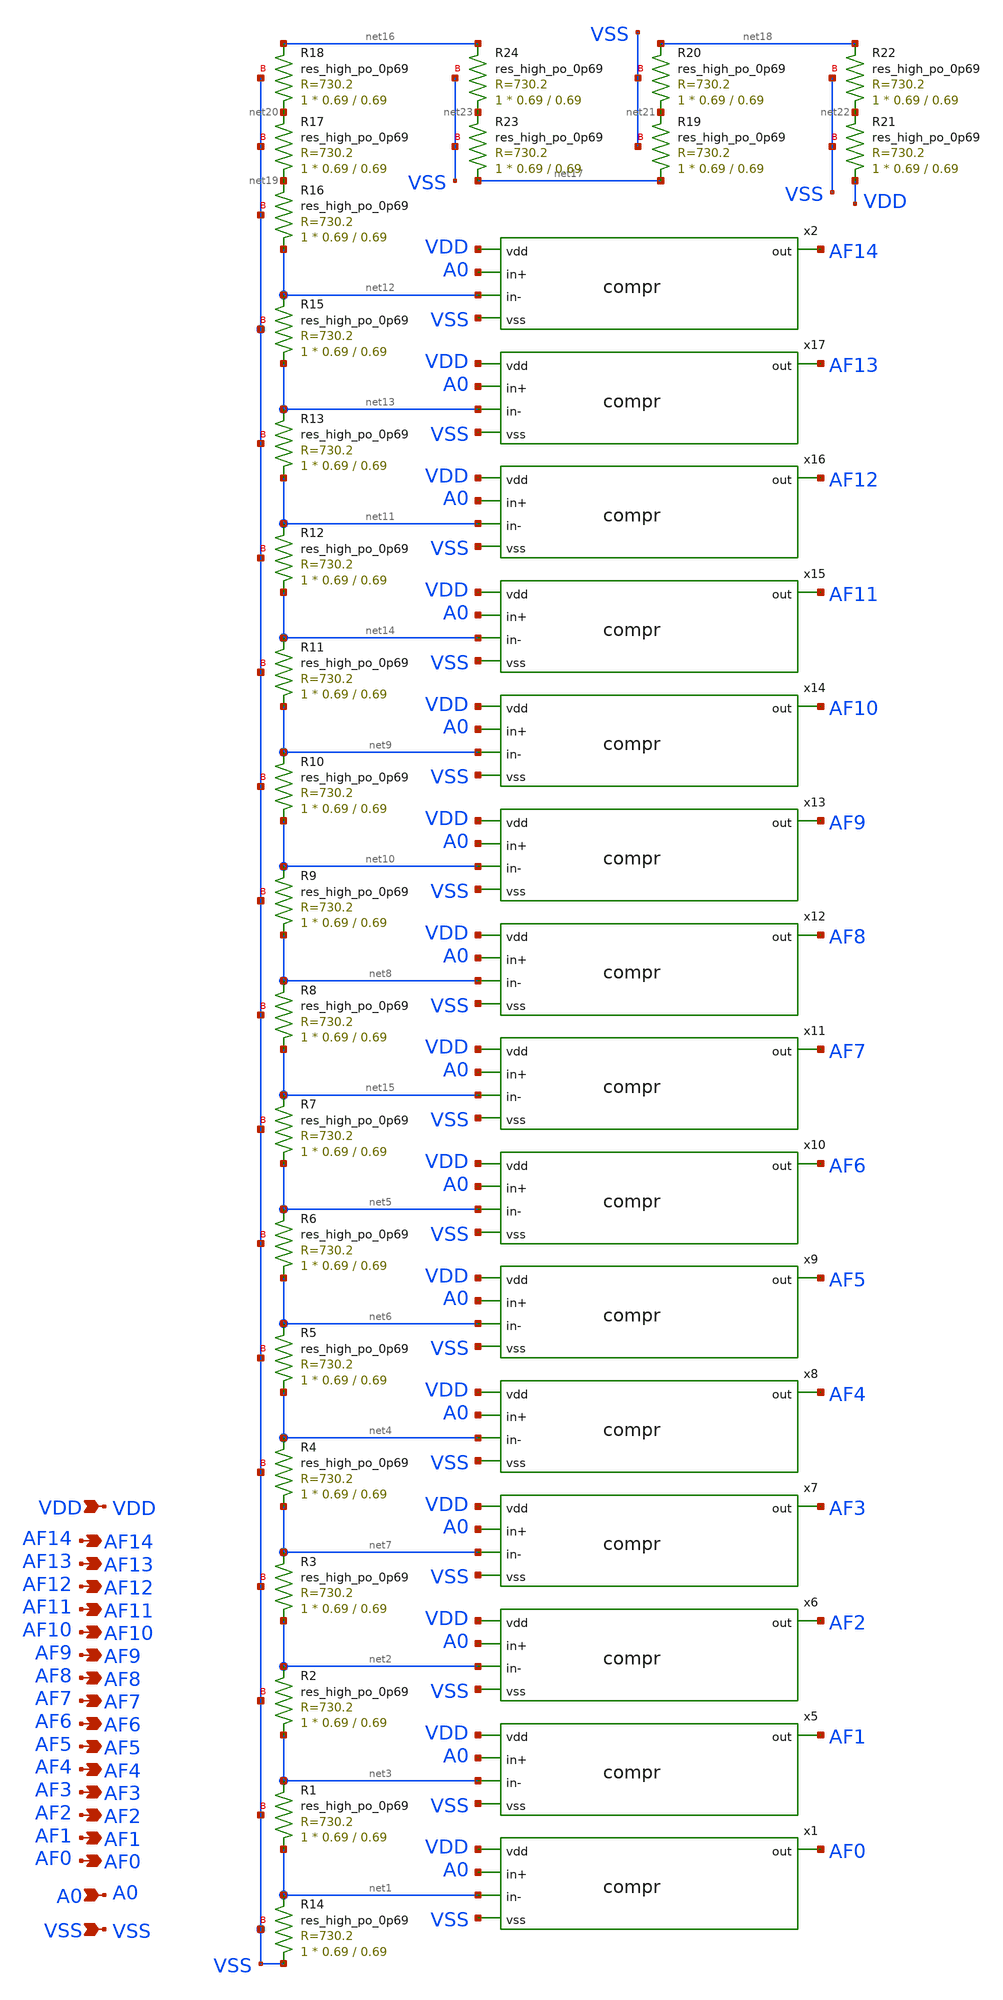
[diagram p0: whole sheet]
** sch_path: xschem/flash_adc.sch
**.subckt flash_adc VDD VSS A0 AF3 AF2 AF1 AF0 AF7 AF6 AF5 AF4 AF11 AF10 AF9 AF8 AF14 AF13 AF12
*.ipin VDD
*.ipin VSS
*.ipin A0
*.opin AF3
*.opin AF2
*.opin AF1
*.opin AF0
*.opin AF7
*.opin AF6
*.opin AF5
*.opin AF4
*.opin AF11
*.opin AF10
*.opin AF9
*.opin AF8
*.opin AF14
*.opin AF13
*.opin AF12
XR14 VSS net1 VSS sky130_fd_pr__res_high_po_0p69 L=0.69 mult=1 m=1
x5 AF1 VDD A0 net3 VSS compr
XR1 net1 net3 VSS sky130_fd_pr__res_high_po_0p69 L=0.69 mult=1 m=1
x6 AF2 VDD A0 net2 VSS compr
XR2 net3 net2 VSS sky130_fd_pr__res_high_po_0p69 L=0.69 mult=1 m=1
x7 AF3 VDD A0 net7 VSS compr
XR3 net2 net7 VSS sky130_fd_pr__res_high_po_0p69 L=0.69 mult=1 m=1
x8 AF4 VDD A0 net4 VSS compr
XR4 net7 net4 VSS sky130_fd_pr__res_high_po_0p69 L=0.69 mult=1 m=1
x9 AF5 VDD A0 net6 VSS compr
XR5 net4 net6 VSS sky130_fd_pr__res_high_po_0p69 L=0.69 mult=1 m=1
x10 AF6 VDD A0 net5 VSS compr
XR6 net6 net5 VSS sky130_fd_pr__res_high_po_0p69 L=0.69 mult=1 m=1
x11 AF7 VDD A0 net15 VSS compr
XR7 net5 net15 VSS sky130_fd_pr__res_high_po_0p69 L=0.69 mult=1 m=1
x12 AF8 VDD A0 net8 VSS compr
XR8 net15 net8 VSS sky130_fd_pr__res_high_po_0p69 L=0.69 mult=1 m=1
x13 AF9 VDD A0 net10 VSS compr
XR9 net8 net10 VSS sky130_fd_pr__res_high_po_0p69 L=0.69 mult=1 m=1
x14 AF10 VDD A0 net9 VSS compr
XR10 net10 net9 VSS sky130_fd_pr__res_high_po_0p69 L=0.69 mult=1 m=1
x15 AF11 VDD A0 net14 VSS compr
XR11 net9 net14 VSS sky130_fd_pr__res_high_po_0p69 L=0.69 mult=1 m=1
x16 AF12 VDD A0 net11 VSS compr
XR12 net14 net11 VSS sky130_fd_pr__res_high_po_0p69 L=0.69 mult=1 m=1
x17 AF13 VDD A0 net13 VSS compr
XR13 net11 net13 VSS sky130_fd_pr__res_high_po_0p69 L=0.69 mult=1 m=1
XR15 net13 net12 VSS sky130_fd_pr__res_high_po_0p69 L=0.69 mult=1 m=1
XR16 net12 net19 VSS sky130_fd_pr__res_high_po_0p69 L=0.69 mult=1 m=1
XR17 net19 net20 VSS sky130_fd_pr__res_high_po_0p69 L=0.69 mult=1 m=1
XR18 net20 net16 VSS sky130_fd_pr__res_high_po_0p69 L=0.69 mult=1 m=1
XR19 net17 net21 VSS sky130_fd_pr__res_high_po_0p69 L=0.69 mult=1 m=1
XR20 net21 net18 VSS sky130_fd_pr__res_high_po_0p69 L=0.69 mult=1 m=1
XR21 VDD net22 VSS sky130_fd_pr__res_high_po_0p69 L=0.69 mult=1 m=1
XR22 net22 net18 VSS sky130_fd_pr__res_high_po_0p69 L=0.69 mult=1 m=1
XR23 net17 net23 VSS sky130_fd_pr__res_high_po_0p69 L=0.69 mult=1 m=1
XR24 net23 net16 VSS sky130_fd_pr__res_high_po_0p69 L=0.69 mult=1 m=1
x1 AF0 VDD A0 net1 VSS compr
x2 AF14 VDD A0 net12 VSS compr
**.ends

* expanding   symbol:  /home/ttuser/Documents/adc_dac_ter_alu/src/xschem/compr.sym # of pins=5
** sym_path: /home/ttuser/Documents/adc_dac_ter_alu/src/xschem/compr.sym
** sch_path: /home/ttuser/Documents/adc_dac_ter_alu/src/xschem/compr.sch
.subckt compr out vdd in+ in- vss
*.ipin IN+
*.opin OUT
*.ipin IN-
*.ipin VDD
*.ipin VSS
XM1 VSS net2 net2 VSS sky130_fd_pr__nfet_01v8_lvt L=4 W=2 nf=1 ad='int((nf+1)/2) * W/nf * 0.29' as='int((nf+2)/2) * W/nf * 0.29'
+ pd='2*int((nf+1)/2) * (W/nf + 0.29)' ps='2*int((nf+2)/2) * (W/nf + 0.29)' nrd='0.29 / W' nrs='0.29 / W'
+ sa=0 sb=0 sd=0 mult=1 m=1
XM2 VSS g1 g1 VSS sky130_fd_pr__nfet_01v8_lvt L=4 W=2 nf=1 ad='int((nf+1)/2) * W/nf * 0.29' as='int((nf+2)/2) * W/nf * 0.29'
+ pd='2*int((nf+1)/2) * (W/nf + 0.29)' ps='2*int((nf+2)/2) * (W/nf + 0.29)' nrd='0.29 / W' nrs='0.29 / W'
+ sa=0 sb=0 sd=0 mult=1 m=1
XM3 VSS net2 net4 VSS sky130_fd_pr__nfet_01v8_lvt L=4 W=2 nf=1 ad='int((nf+1)/2) * W/nf * 0.29' as='int((nf+2)/2) * W/nf * 0.29'
+ pd='2*int((nf+1)/2) * (W/nf + 0.29)' ps='2*int((nf+2)/2) * (W/nf + 0.29)' nrd='0.29 / W' nrs='0.29 / W'
+ sa=0 sb=0 sd=0 mult=1 m=1
XM4 VSS g1 net3 VSS sky130_fd_pr__nfet_01v8_lvt L=4 W=2 nf=1 ad='int((nf+1)/2) * W/nf * 0.29' as='int((nf+2)/2) * W/nf * 0.29'
+ pd='2*int((nf+1)/2) * (W/nf + 0.29)' ps='2*int((nf+2)/2) * (W/nf + 0.29)' nrd='0.29 / W' nrs='0.29 / W'
+ sa=0 sb=0 sd=0 mult=1 m=1
XM5 net2 IN+ net1 VDD sky130_fd_pr__pfet_01v8_lvt L=2 W=8 nf=1 ad='int((nf+1)/2) * W/nf * 0.29' as='int((nf+2)/2) * W/nf * 0.29'
+ pd='2*int((nf+1)/2) * (W/nf + 0.29)' ps='2*int((nf+2)/2) * (W/nf + 0.29)' nrd='0.29 / W' nrs='0.29 / W'
+ sa=0 sb=0 sd=0 mult=1 m=1
XM6 g1 IN- net1 VDD sky130_fd_pr__pfet_01v8_lvt L=2 W=8 nf=1 ad='int((nf+1)/2) * W/nf * 0.29' as='int((nf+2)/2) * W/nf * 0.29'
+ pd='2*int((nf+1)/2) * (W/nf + 0.29)' ps='2*int((nf+2)/2) * (W/nf + 0.29)' nrd='0.29 / W' nrs='0.29 / W'
+ sa=0 sb=0 sd=0 mult=1 m=1
XM7 net4 net3 net5 VDD sky130_fd_pr__pfet_01v8_lvt L=4 W=4 nf=1 ad='int((nf+1)/2) * W/nf * 0.29' as='int((nf+2)/2) * W/nf * 0.29'
+ pd='2*int((nf+1)/2) * (W/nf + 0.29)' ps='2*int((nf+2)/2) * (W/nf + 0.29)' nrd='0.29 / W' nrs='0.29 / W'
+ sa=0 sb=0 sd=0 mult=1 m=1
XM9 net3 net3 net5 VDD sky130_fd_pr__pfet_01v8_lvt L=4 W=4 nf=1 ad='int((nf+1)/2) * W/nf * 0.29' as='int((nf+2)/2) * W/nf * 0.29'
+ pd='2*int((nf+1)/2) * (W/nf + 0.29)' ps='2*int((nf+2)/2) * (W/nf + 0.29)' nrd='0.29 / W' nrs='0.29 / W'
+ sa=0 sb=0 sd=0 mult=1 m=1
XM8 net1 VSS VDD VDD sky130_fd_pr__pfet_01v8 L=8 W=2 nf=1 ad='int((nf+1)/2) * W/nf * 0.29' as='int((nf+2)/2) * W/nf * 0.29'
+ pd='2*int((nf+1)/2) * (W/nf + 0.29)' ps='2*int((nf+2)/2) * (W/nf + 0.29)' nrd='0.29 / W' nrs='0.29 / W'
+ sa=0 sb=0 sd=0 mult=1 m=1
XM10 net5 VSS VDD VDD sky130_fd_pr__pfet_01v8 L=0.15 W=5 nf=1 ad='int((nf+1)/2) * W/nf * 0.29' as='int((nf+2)/2) * W/nf * 0.29'
+ pd='2*int((nf+1)/2) * (W/nf + 0.29)' ps='2*int((nf+2)/2) * (W/nf + 0.29)' nrd='0.29 / W' nrs='0.29 / W'
+ sa=0 sb=0 sd=0 mult=1 m=1
XM14 OUT net6 VSS VSS sky130_fd_pr__nfet_01v8 L=0.15 W=2 nf=1 ad='int((nf+1)/2) * W/nf * 0.29' as='int((nf+2)/2) * W/nf * 0.29'
+ pd='2*int((nf+1)/2) * (W/nf + 0.29)' ps='2*int((nf+2)/2) * (W/nf + 0.29)' nrd='0.29 / W' nrs='0.29 / W'
+ sa=0 sb=0 sd=0 mult=1 m=1
XM13 OUT net6 VDD VDD sky130_fd_pr__pfet_01v8 L=0.15 W=8 nf=1 ad='int((nf+1)/2) * W/nf * 0.29' as='int((nf+2)/2) * W/nf * 0.29'
+ pd='2*int((nf+1)/2) * (W/nf + 0.29)' ps='2*int((nf+2)/2) * (W/nf + 0.29)' nrd='0.29 / W' nrs='0.29 / W'
+ sa=0 sb=0 sd=0 mult=1 m=1
XM11 net6 net4 VSS VSS sky130_fd_pr__nfet_01v8 L=0.15 W=1 nf=1 ad='int((nf+1)/2) * W/nf * 0.29' as='int((nf+2)/2) * W/nf * 0.29'
+ pd='2*int((nf+1)/2) * (W/nf + 0.29)' ps='2*int((nf+2)/2) * (W/nf + 0.29)' nrd='0.29 / W' nrs='0.29 / W'
+ sa=0 sb=0 sd=0 mult=1 m=1
XM12 net6 net4 VDD VDD sky130_fd_pr__pfet_01v8 L=0.15 W=3 nf=1 ad='int((nf+1)/2) * W/nf * 0.29' as='int((nf+2)/2) * W/nf * 0.29'
+ pd='2*int((nf+1)/2) * (W/nf + 0.29)' ps='2*int((nf+2)/2) * (W/nf + 0.29)' nrd='0.29 / W' nrs='0.29 / W'
+ sa=0 sb=0 sd=0 mult=1 m=1
.ends

.end
